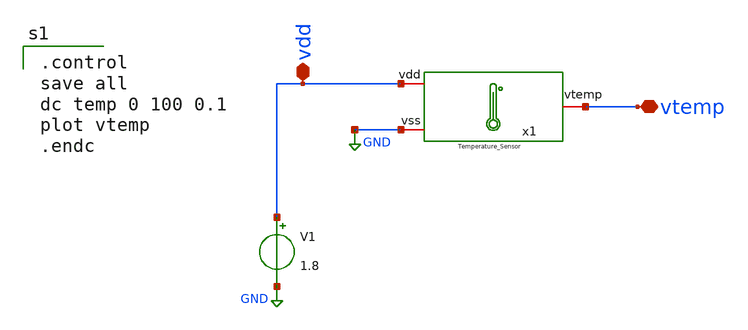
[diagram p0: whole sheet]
** sch_path: XSCHEM/Temp_Sensor_tb.sch
**.subckt Temp_Sensor_tb vdd vtemp
*.iopin vdd
*.iopin vtemp
V1 vdd GND 1.8
x1 vdd vtemp GND Temperature_Sensor
**** begin user architecture code

** opencircuitdesign pdks install
.lib $::SKYWATER_MODELS/sky130.lib.spice tt



.control
save all
dc temp 0 100 0.1
plot vtemp
.endc

**** end user architecture code
**.ends

* expanding   symbol:  Documentos/TESIS DE
*+ GRADO/WORK_IN_PROGRESS/My_xschem_prueba/Temperature_Sensor.sym # of pins=3
** sym_path: XSCHEM/Temperature_Sensor.sym
** sch_path: XSCHEM/Temperature_Sensor.sch
.subckt Temperature_Sensor vdd vtemp vss
*.iopin vdd
*.iopin vss
*.iopin vtemp
XM8 net1 net4 net2 vss sky130_fd_pr__nfet_01v8_lvt L=2 W=1 nf=1 ad='int((nf+1)/2) * W/nf * 0.29' as='int((nf+2)/2) * W/nf * 0.29'
+ pd='2*int((nf+1)/2) * (W/nf + 0.29)' ps='2*int((nf+2)/2) * (W/nf + 0.29)' nrd='0.29 / W' nrs='0.29 / W'
+ sa=0 sb=0 sd=0 mult=4 m=4
XM9 vtemp net3 net2 vss sky130_fd_pr__nfet_01v8_lvt L=0.5 W=1 nf=1 ad='int((nf+1)/2) * W/nf * 0.29' as='int((nf+2)/2) * W/nf * 0.29'
+ pd='2*int((nf+1)/2) * (W/nf + 0.29)' ps='2*int((nf+2)/2) * (W/nf + 0.29)' nrd='0.29 / W' nrs='0.29 / W'
+ sa=0 sb=0 sd=0 mult=4 m=4
XM10 net2 net5 vss vss sky130_fd_pr__nfet_01v8 L=2 W=5 nf=1 ad='int((nf+1)/2) * W/nf * 0.29' as='int((nf+2)/2) * W/nf * 0.29'
+ pd='2*int((nf+1)/2) * (W/nf + 0.29)' ps='2*int((nf+2)/2) * (W/nf + 0.29)' nrd='0.29 / W' nrs='0.29 / W'
+ sa=0 sb=0 sd=0 mult=4 m=4
XM11 net1 net1 vdd vdd sky130_fd_pr__pfet_01v8_lvt L=2 W=5 nf=1 ad='int((nf+1)/2) * W/nf * 0.29' as='int((nf+2)/2) * W/nf * 0.29'
+ pd='2*int((nf+1)/2) * (W/nf + 0.29)' ps='2*int((nf+2)/2) * (W/nf + 0.29)' nrd='0.29 / W' nrs='0.29 / W'
+ sa=0 sb=0 sd=0 mult=4 m=4
XM12 vtemp net1 vdd vdd sky130_fd_pr__pfet_01v8_lvt L=2 W=5 nf=1 ad='int((nf+1)/2) * W/nf * 0.29' as='int((nf+2)/2) * W/nf * 0.29'
+ pd='2*int((nf+1)/2) * (W/nf + 0.29)' ps='2*int((nf+2)/2) * (W/nf + 0.29)' nrd='0.29 / W' nrs='0.29 / W'
+ sa=0 sb=0 sd=0 mult=4 m=4
XM13 net6 net6 net4 vss sky130_fd_pr__nfet_01v8_lvt L=2 W=4 nf=1 ad='int((nf+1)/2) * W/nf * 0.29' as='int((nf+2)/2) * W/nf * 0.29'
+ pd='2*int((nf+1)/2) * (W/nf + 0.29)' ps='2*int((nf+2)/2) * (W/nf + 0.29)' nrd='0.29 / W' nrs='0.29 / W'
+ sa=0 sb=0 sd=0 mult=1 m=1
XQ3 vss vss net4 sky130_fd_pr__pnp_05v5_W3p40L3p40 m=1
XM14 vdd net6 net3 vss sky130_fd_pr__nfet_01v8_lvt L=2 W=4 nf=1 ad='int((nf+1)/2) * W/nf * 0.29' as='int((nf+2)/2) * W/nf * 0.29'
+ pd='2*int((nf+1)/2) * (W/nf + 0.29)' ps='2*int((nf+2)/2) * (W/nf + 0.29)' nrd='0.29 / W' nrs='0.29 / W'
+ sa=0 sb=0 sd=0 mult=10 m=10
XQ4 vss vss net3 sky130_fd_pr__pnp_05v5_W3p40L3p40 m=1
XM7 net6 net5 vdd vdd sky130_fd_pr__pfet_01v8_lvt L=2 W=2 nf=1 ad='int((nf+1)/2) * W/nf * 0.29' as='int((nf+2)/2) * W/nf * 0.29'
+ pd='2*int((nf+1)/2) * (W/nf + 0.29)' ps='2*int((nf+2)/2) * (W/nf + 0.29)' nrd='0.29 / W' nrs='0.29 / W'
+ sa=0 sb=0 sd=0 mult=1 m=1
XM20 net7 net7 vdd vdd sky130_fd_pr__pfet_01v8_lvt L=2 W=2 nf=1 ad='int((nf+1)/2) * W/nf * 0.29' as='int((nf+2)/2) * W/nf * 0.29'
+ pd='2*int((nf+1)/2) * (W/nf + 0.29)' ps='2*int((nf+2)/2) * (W/nf + 0.29)' nrd='0.29 / W' nrs='0.29 / W'
+ sa=0 sb=0 sd=0 mult=1 m=1
XM21 net5 net5 vss vss sky130_fd_pr__nfet_01v8_lvt L=2 W=0.5 nf=1 ad='int((nf+1)/2) * W/nf * 0.29' as='int((nf+2)/2) * W/nf * 0.29'
+ pd='2*int((nf+1)/2) * (W/nf + 0.29)' ps='2*int((nf+2)/2) * (W/nf + 0.29)' nrd='0.29 / W' nrs='0.29 / W'
+ sa=0 sb=0 sd=0 mult=1 m=1
XM22 net8 net7 vdd vdd sky130_fd_pr__pfet_01v8_lvt L=2 W=2 nf=1 ad='int((nf+1)/2) * W/nf * 0.29' as='int((nf+2)/2) * W/nf * 0.29'
+ pd='2*int((nf+1)/2) * (W/nf + 0.29)' ps='2*int((nf+2)/2) * (W/nf + 0.29)' nrd='0.29 / W' nrs='0.29 / W'
+ sa=0 sb=0 sd=0 mult=1 m=1
XM23 net9 net5 net8 vdd sky130_fd_pr__pfet_01v8_lvt L=2 W=2 nf=1 ad='int((nf+1)/2) * W/nf * 0.29' as='int((nf+2)/2) * W/nf * 0.29'
+ pd='2*int((nf+1)/2) * (W/nf + 0.29)' ps='2*int((nf+2)/2) * (W/nf + 0.29)' nrd='0.29 / W' nrs='0.29 / W'
+ sa=0 sb=0 sd=0 mult=1 m=1
XM24 net5 net5 net7 vdd sky130_fd_pr__pfet_01v8_lvt L=2 W=2 nf=1 ad='int((nf+1)/2) * W/nf * 0.29' as='int((nf+2)/2) * W/nf * 0.29'
+ pd='2*int((nf+1)/2) * (W/nf + 0.29)' ps='2*int((nf+2)/2) * (W/nf + 0.29)' nrd='0.29 / W' nrs='0.29 / W'
+ sa=0 sb=0 sd=0 mult=1 m=1
XM25 net9 net9 vss vss sky130_fd_pr__nfet_01v8_lvt L=2 W=0.5 nf=1 ad='int((nf+1)/2) * W/nf * 0.29' as='int((nf+2)/2) * W/nf * 0.29'
+ pd='2*int((nf+1)/2) * (W/nf + 0.29)' ps='2*int((nf+2)/2) * (W/nf + 0.29)' nrd='0.29 / W' nrs='0.29 / W'
+ sa=0 sb=0 sd=0 mult=1 m=1
.ends

.GLOBAL GND
.end
